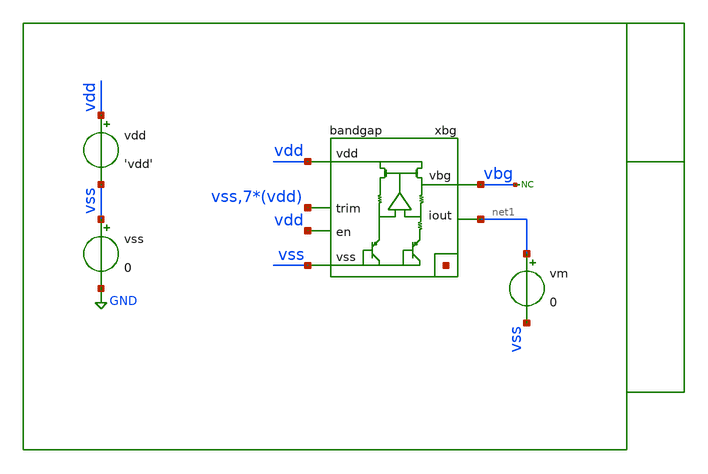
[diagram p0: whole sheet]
** sch_path: xschem/tb/bandgap_cm/bandgap/dc_bandgap_temperature.sch
**.subckt dc_bandgap_temperature
xbg vdd vbg vss net2[7] net2[6] net2[5] net2[4] net2[3] net2[2] net2[1] net2[0] vss vdd vdd vdd vdd
+ vdd vdd vdd net1 vdd bandgap
vdd vdd vss 'vdd'
vss vss GND 0
* noconn vbg
vm net1 vss 0
**** begin user architecture code

* Control

.param vdd = 3.3
.temp 27

.options reltol   = 1e-6
.options seed     = 3


.control
save all

let tempmin = -40
let tempmax = 85
let tempstep = 5

let tmeasmin = tempmin + 1
let tmeasmax = tempmax - 1

dc temp $&tempmin $&tempmax $&tempstep

gnuplot p1 vbg

meas dc vbg_min min vbg from=tmeasmin to=tmeasmax
meas dc vbg_max max vbg from=tmeasmin to=tmeasmax

let vbg_min_eval = vbg_min + 1u
let vbg_max_eval = vbg_max - 1u

meas dc t_max when v(vbg)=vbg_max_eval
meas dc t_min when v(vbg)=vbg_min_eval

let dv_dT = (vbg_max-vbg_min)/abs((t_max-t_min))

let iout = abs(vm#branch)

gnuplot p2 iout

print vbg_min
print vbg_max
print t_min
print t_max
print dv_dT

set wr_singlescale
set wr_vecnames
wrdata data.csv vbg
.endc
.end


 * Model Corners

.include $::CORNERS/ngspice/tt.spice
*.include $::CORNERS/ngspice/ff.spice
*.include $::CORNERS/ngspice/ss.spice
*.include $::CORNERS/ngspice/sf.spice
*.include $::CORNERS/ngspice/fs.spice

**** end user architecture code
**.ends
.GLOBAL GND
.end
